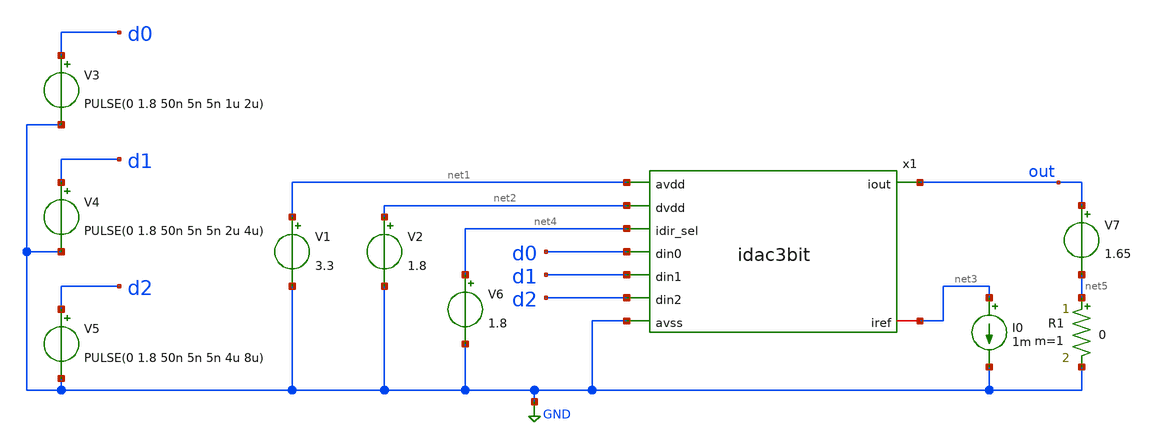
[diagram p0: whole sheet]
** sch_path: xschem/idac3bit_tb.sch
**.subckt idac3bit_tb
x1 net1 out net2 d0 net4 d1 GND d2 net3 idac3bit
V1 net1 GND 3.3
V2 net2 GND 1.8
I0 net3 GND 1m
V3 d0 GND PULSE(0 1.8 50n 5n 5n 1u 2u)
V4 d1 GND PULSE(0 1.8 50n 5n 5n 2u 4u)
V5 d2 GND PULSE(0 1.8 50n 5n 5n 4u 8u)
V6 net4 GND 1.8
V7 out net5 1.65
R1 net5 GND 0 m=1
**** begin user architecture code
 .lib $::SKYWATER_MODELS/sky130.lib.spice tt
.include $::SKYWATER_STDCELLS/../../sky130_fd_sc_hvl/spice/sky130_fd_sc_hvl.spice

.param mc_mm_switch=0
.param mc_pr_switch=1



.option wnflag=0
.option savecurrents
.control
save all
tran 10n 20u
plot i(V7)
write currentmirrortb.raw
op
.endc


**** end user architecture code
**.ends
.GLOBAL GND
.end
